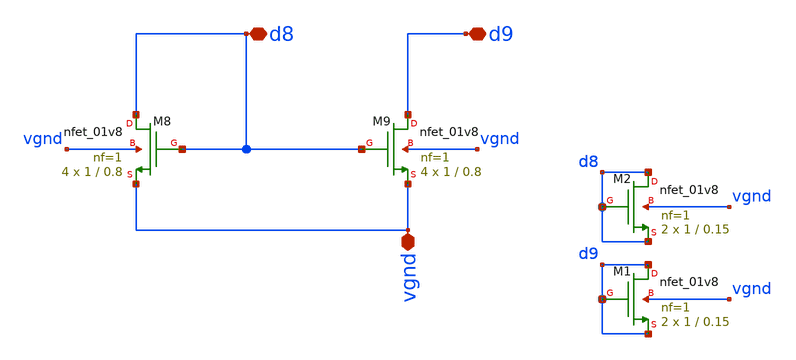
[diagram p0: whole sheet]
** sch_path: mag/nmos_dif.sch
**.subckt nmos_dif vgnd d9 d8
*.iopin vgnd
*.iopin d9
*.iopin d8
XM8 d8 d8 vgnd vgnd sky130_fd_pr__nfet_01v8 L=0.8 W=1 nf=1 ad='int((nf+1)/2) * W/nf * 0.29' as='int((nf+2)/2) * W/nf * 0.29'
+ pd='2*int((nf+1)/2) * (W/nf + 0.29)' ps='2*int((nf+2)/2) * (W/nf + 0.29)' nrd='0.29 / W' nrs='0.29 / W'
+ sa=0 sb=0 sd=0 mult=4 m=4
XM9 d9 d8 vgnd vgnd sky130_fd_pr__nfet_01v8 L=0.8 W=1 nf=1 ad='int((nf+1)/2) * W/nf * 0.29' as='int((nf+2)/2) * W/nf * 0.29'
+ pd='2*int((nf+1)/2) * (W/nf + 0.29)' ps='2*int((nf+2)/2) * (W/nf + 0.29)' nrd='0.29 / W' nrs='0.29 / W'
+ sa=0 sb=0 sd=0 mult=4 m=4
XM1 d9 d9 d9 vgnd sky130_fd_pr__nfet_01v8 L=0.15 W=1 nf=1 ad='int((nf+1)/2) * W/nf * 0.29' as='int((nf+2)/2) * W/nf * 0.29'
+ pd='2*int((nf+1)/2) * (W/nf + 0.29)' ps='2*int((nf+2)/2) * (W/nf + 0.29)' nrd='0.29 / W' nrs='0.29 / W'
+ sa=0 sb=0 sd=0 mult=2 m=2
XM2 d8 d8 d8 vgnd sky130_fd_pr__nfet_01v8 L=0.15 W=1 nf=1 ad='int((nf+1)/2) * W/nf * 0.29' as='int((nf+2)/2) * W/nf * 0.29'
+ pd='2*int((nf+1)/2) * (W/nf + 0.29)' ps='2*int((nf+2)/2) * (W/nf + 0.29)' nrd='0.29 / W' nrs='0.29 / W'
+ sa=0 sb=0 sd=0 mult=2 m=2
**.ends
.end
